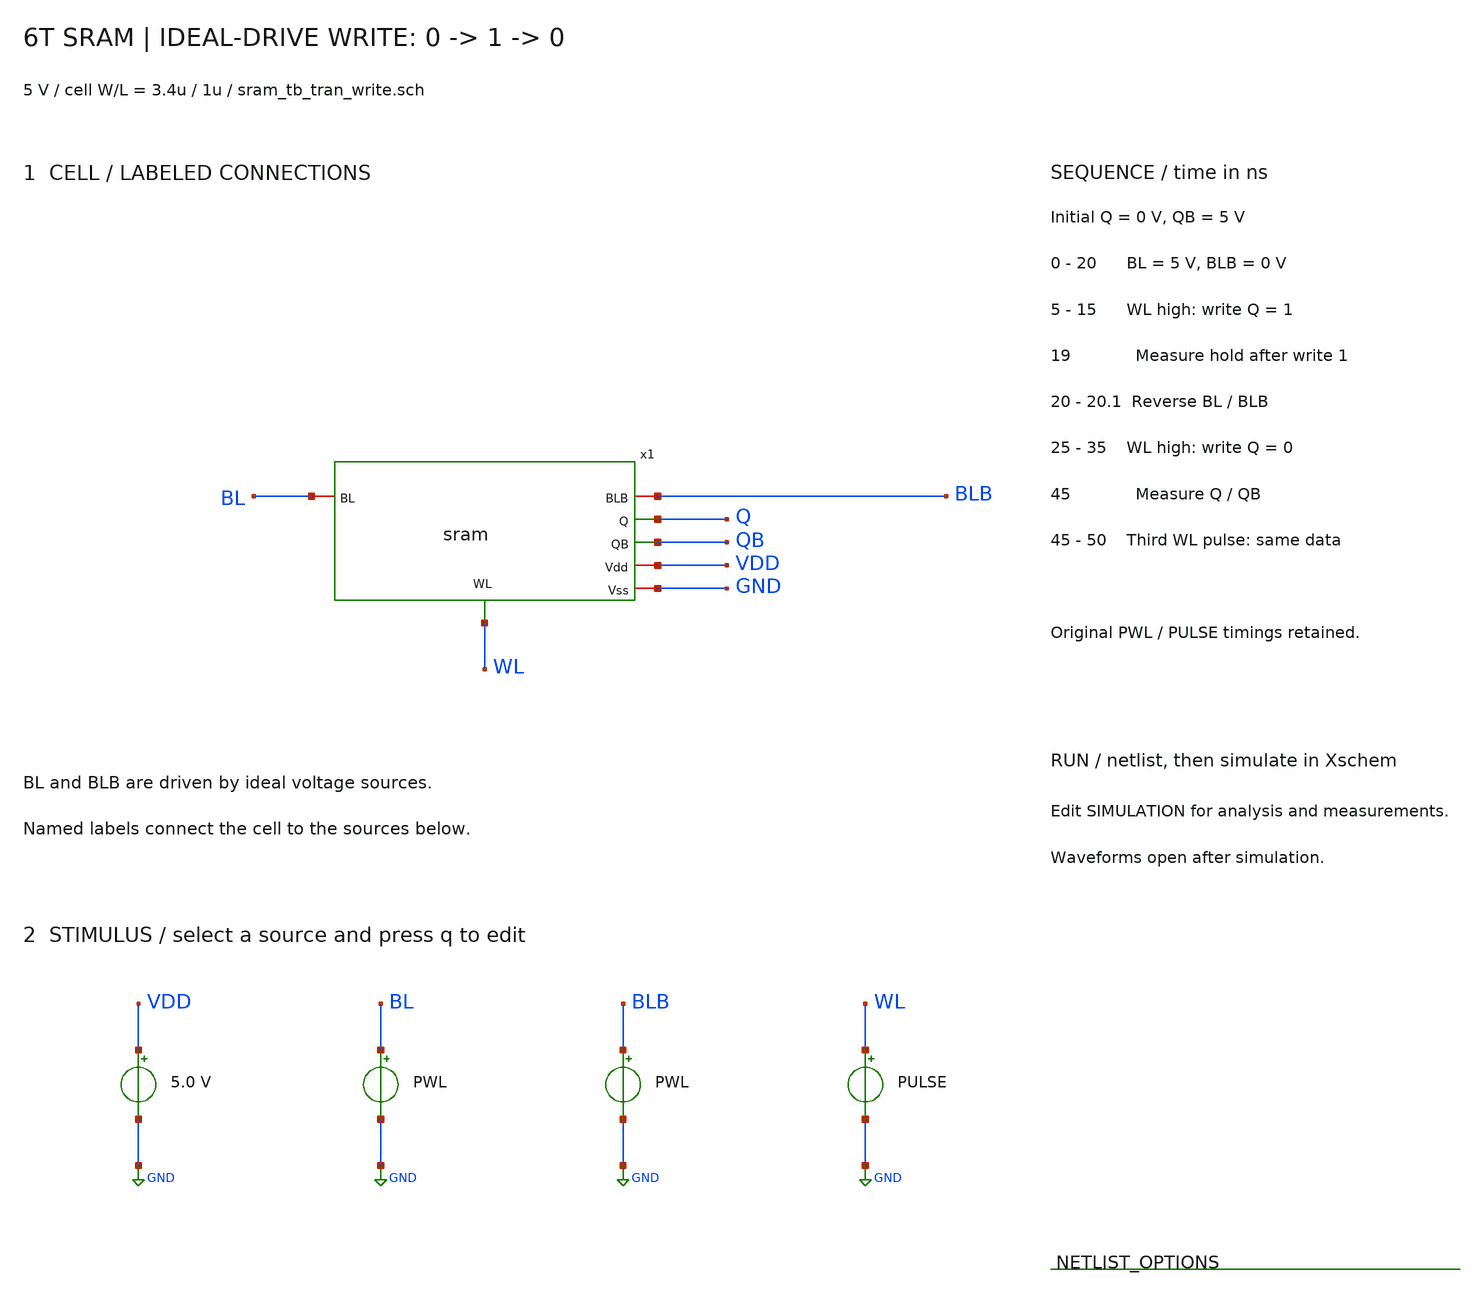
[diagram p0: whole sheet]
** sch_path: member_project/SRAM/PenguinEino/learning/schematics/sram_tb_tran_write.sch
**.subckt sram_tb_tran_write
x1 WL VDD BLB Q QB BL GND sram
Vdd VDD GND 5.0
VBL BL GND PWL(0 5 20n 5 20.1n 0 50n 0)
VBLB BLB GND PWL(0 0 20n 0 20.1n 5 50n 5)
VWL WL GND PULSE(0 5 5n 0.1n 0.1n 10n 20n)
**** begin user architecture code
 .include $::LIB/ip62_models

.ic v(Q) = 0 v(QB)=5

.control
save all

tran 0.05n 50n

meas tran T_write_5 trig v(WL) val=2.5 rise=1 targ v(Q) val=2.5 rise=1
meas tran Q_hold_5 find v(Q) at=19n
meas tran QB_hold_5 find v(QB) at=19n
meas tran T_write_0 trig v(WL) val=2.5 rise=2 targ v(Q) val=2.5 fall=1
meas tran Q_hold_0 find v(Q) at=45n
meas tran QB_hold_0 find v(QB) at=45n

plot v(Q) v(QB) ylimit -0.5 5.5 title 'CELL: ideal-drive write 1 then write 0'
plot v(BL) v(BLB) ylimit -0.5 5.5 title 'BITLINES: ideal voltage sources'
plot v(WL) ylimit -0.5 5.5 title 'WORD LINE'
.endc

**** end user architecture code
**.ends
.GLOBAL GND
.end
